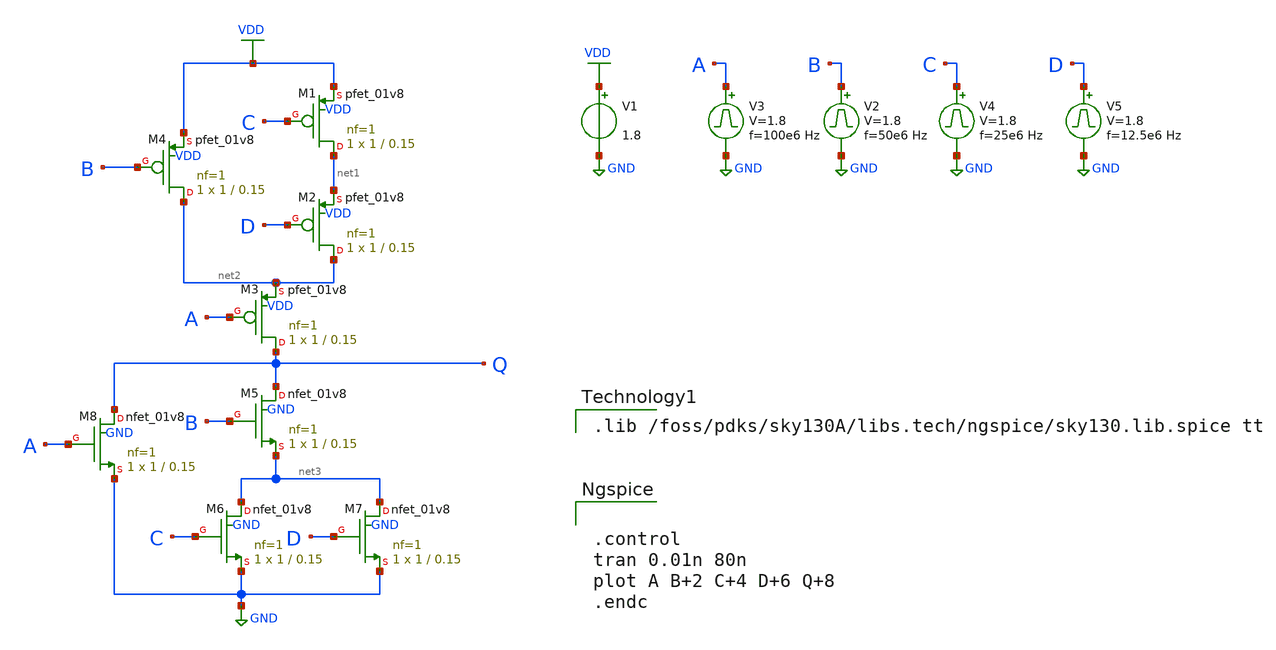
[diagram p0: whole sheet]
** sch_path: Modulo_Digital/Lab1/cmos_funct1.sch
**.subckt cmos_funct1
XM4 net2 B VDD VDD sky130_fd_pr__pfet_01v8 L=0.15 W=1 nf=1 ad='int((1 + 1)/2) * 1 / 1 * 0.29' as='int((1 + 2)/2) * 1 / 1 * 0.29'
+ pd='2*int((1 + 1)/2) * (1 / 1 + 0.29)' ps='2*int((1 + 2)/2) * (1 / 1 + 0.29)' nrd='0.29 / 1 ' nrs='0.29 / 1 '
+ sa=0 sb=0 sd=0 mult=1 m=1
XM8 Q A GND GND sky130_fd_pr__nfet_01v8 L=0.15 W=1 nf=1 ad='int((nf+1)/2) * W/nf * 0.29' as='int((nf+2)/2) * W/nf * 0.29'
+ pd='2*int((nf+1)/2) * (W/nf + 0.29)' ps='2*int((nf+2)/2) * (W/nf + 0.29)' nrd='0.29 / W' nrs='0.29 / W'
+ sa=0 sb=0 sd=0 mult=1 m=1
XM1 net1 C VDD VDD sky130_fd_pr__pfet_01v8 L=0.15 W=1 nf=1 ad='int((1 + 1)/2) * 1 / 1 * 0.29' as='int((1 + 2)/2) * 1 / 1 * 0.29'
+ pd='2*int((1 + 1)/2) * (1 / 1 + 0.29)' ps='2*int((1 + 2)/2) * (1 / 1 + 0.29)' nrd='0.29 / 1 ' nrs='0.29 / 1 '
+ sa=0 sb=0 sd=0 mult=1 m=1
XM2 net2 D net1 VDD sky130_fd_pr__pfet_01v8 L=0.15 W=1 nf=1 ad='int((1 + 1)/2) * 1 / 1 * 0.29' as='int((1 + 2)/2) * 1 / 1 * 0.29'
+ pd='2*int((1 + 1)/2) * (1 / 1 + 0.29)' ps='2*int((1 + 2)/2) * (1 / 1 + 0.29)' nrd='0.29 / 1 ' nrs='0.29 / 1 '
+ sa=0 sb=0 sd=0 mult=1 m=1
XM3 Q A net2 VDD sky130_fd_pr__pfet_01v8 L=0.15 W=1 nf=1 ad='int((1 + 1)/2) * 1 / 1 * 0.29' as='int((1 + 2)/2) * 1 / 1 * 0.29'
+ pd='2*int((1 + 1)/2) * (1 / 1 + 0.29)' ps='2*int((1 + 2)/2) * (1 / 1 + 0.29)' nrd='0.29 / 1 ' nrs='0.29 / 1 '
+ sa=0 sb=0 sd=0 mult=1 m=1
XM5 Q B net3 GND sky130_fd_pr__nfet_01v8 L=0.15 W=1 nf=1 ad='int((nf+1)/2) * W/nf * 0.29' as='int((nf+2)/2) * W/nf * 0.29'
+ pd='2*int((nf+1)/2) * (W/nf + 0.29)' ps='2*int((nf+2)/2) * (W/nf + 0.29)' nrd='0.29 / W' nrs='0.29 / W'
+ sa=0 sb=0 sd=0 mult=1 m=1
XM6 net3 C GND GND sky130_fd_pr__nfet_01v8 L=0.15 W=1 nf=1 ad='int((nf+1)/2) * W/nf * 0.29' as='int((nf+2)/2) * W/nf * 0.29'
+ pd='2*int((nf+1)/2) * (W/nf + 0.29)' ps='2*int((nf+2)/2) * (W/nf + 0.29)' nrd='0.29 / W' nrs='0.29 / W'
+ sa=0 sb=0 sd=0 mult=1 m=1
XM7 net3 D GND GND sky130_fd_pr__nfet_01v8 L=0.15 W=1 nf=1 ad='int((nf+1)/2) * W/nf * 0.29' as='int((nf+2)/2) * W/nf * 0.29'
+ pd='2*int((nf+1)/2) * (W/nf + 0.29)' ps='2*int((nf+2)/2) * (W/nf + 0.29)' nrd='0.29 / W' nrs='0.29 / W'
+ sa=0 sb=0 sd=0 mult=1 m=1
V1 VDD GND 1.8
V3 A GND pulse 0 1.8 '0.495/ 100e6 ' '0.01/100e6 ' '0.01/100e6 ' '0.49/100e6 ' '1/100e6 '
V2 B GND pulse 0 1.8 '0.495/ 50e6 ' '0.01/50e6 ' '0.01/50e6 ' '0.49/50e6 ' '1/50e6 '
V4 C GND pulse 0 1.8 '0.495/ 25e6 ' '0.01/25e6 ' '0.01/25e6 ' '0.49/25e6 ' '1/25e6 '
V5 D GND pulse 0 1.8 '0.495/ 12.5e6 ' '0.01/12.5e6 ' '0.01/12.5e6 ' '0.49/12.5e6 ' '1/12.5e6 '
**** begin user architecture code

.lib /foss/pdks/sky130A/libs.tech/ngspice/sky130.lib.spice tt



.control
tran 0.01n 80n
plot A B+2 C+4 D+6 Q+8
.endc

**** end user architecture code
**.ends
.GLOBAL GND
.GLOBAL VDD
.end
